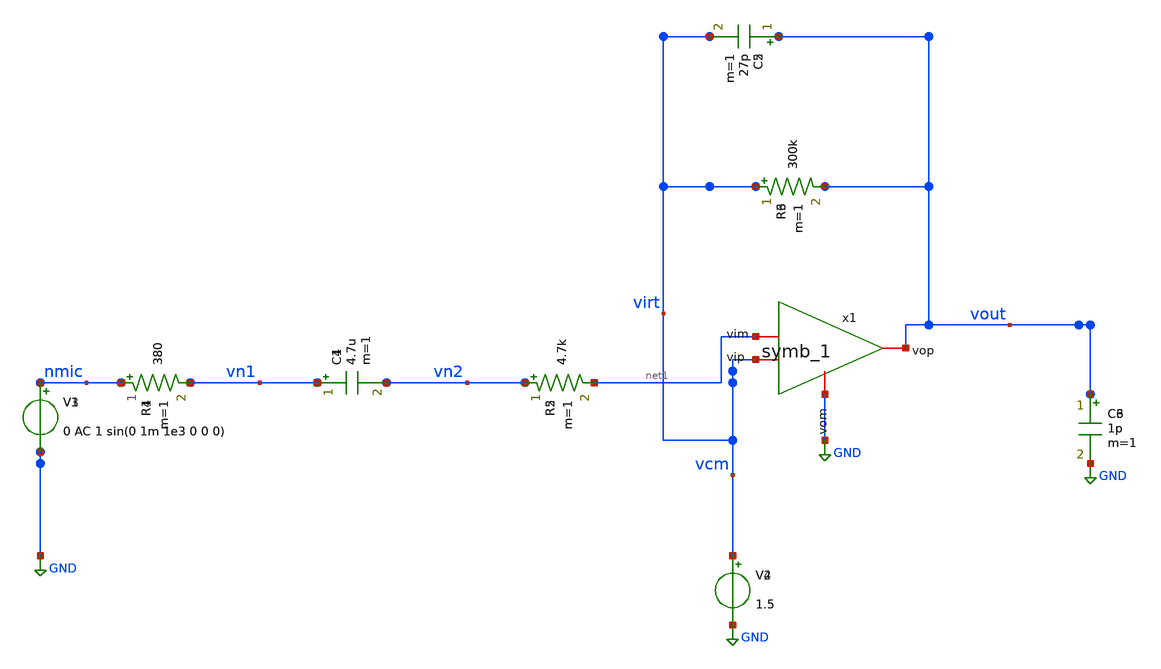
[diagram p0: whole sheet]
** sch_path: xschem/new_op.sch
**.subckt new_op
V1 nmic GND 0 AC 1 sin(0 1m 1e3 0 0 0)
R1 nmic vn1 380 m=1
C1 vn1 vn2 4.7u m=1
R2 vn2 net1 4.7k m=1
R3 virt vout 300k m=1
C2 vout virt 27p m=1
V2 virt GND 1.5
C3 vout GND 1p m=1
V3 nmic GND 0 AC 1 sin(0 1m 1e3 0 0 0)
R4 nmic vn1 380 m=1
C4 vn1 vn2 4.7u m=1
R5 vn2 net1 4.7k m=1
R6 virt vout 300k m=1
C5 vout virt 27p m=1
V4 virt GND 1.5
C6 vout GND 1p m=1
x1 vout virt net1 GND symb_1
**.ends

* expanding   symbol:  symb_1.sym # of pins=4
** sym_path: xschem/symb_1.sym
** sch_path: xschem/symb_1.sch
.subckt symb_1 vop vip vim vom
*.iopin vip
*.iopin vim
*.iopin vop
*.iopin vom
E1 vop vom vip vim 3
.ends

.GLOBAL GND
.end
